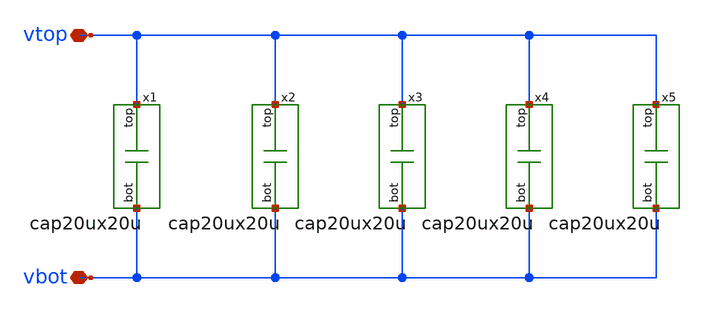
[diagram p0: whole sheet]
** sch_path: v2_feature_extr_withf/mcap_5p.sch
**.subckt mcap_5p vtop vbot
*.iopin vtop
*.iopin vbot
x1 vtop vbot cap20ux20u
x2 vtop vbot cap20ux20u
x3 vtop vbot cap20ux20u
x4 vtop vbot cap20ux20u
x5 vtop vbot cap20ux20u
**.ends
.end
